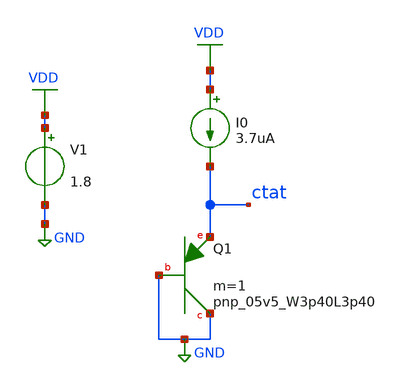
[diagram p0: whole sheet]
** sch_path: xschem/ctat.sch
**.subckt ctat
XQ1 GND GND ctat sky130_fd_pr__pnp_05v5_W3p40L3p40 m=1
I0 VDD ctat 3.7uA
V1 VDD GND 1.8
**** begin user architecture code

** opencircuitdesign pdks install
.lib $::SKYWATER_MODELS/sky130.lib.spice tt




** Analysis Requests **
** Outputs Requests **
.option wnflag=1
.option savecurrents
.control
save all
dc V1 0 1.98 0.01
plot ctat
dc temp -40 125 5
plot ctat
set appendwrite
op
save all
write ctat.raw
.endc


**** end user architecture code
**.ends
.GLOBAL GND
.GLOBAL VDD
.end
